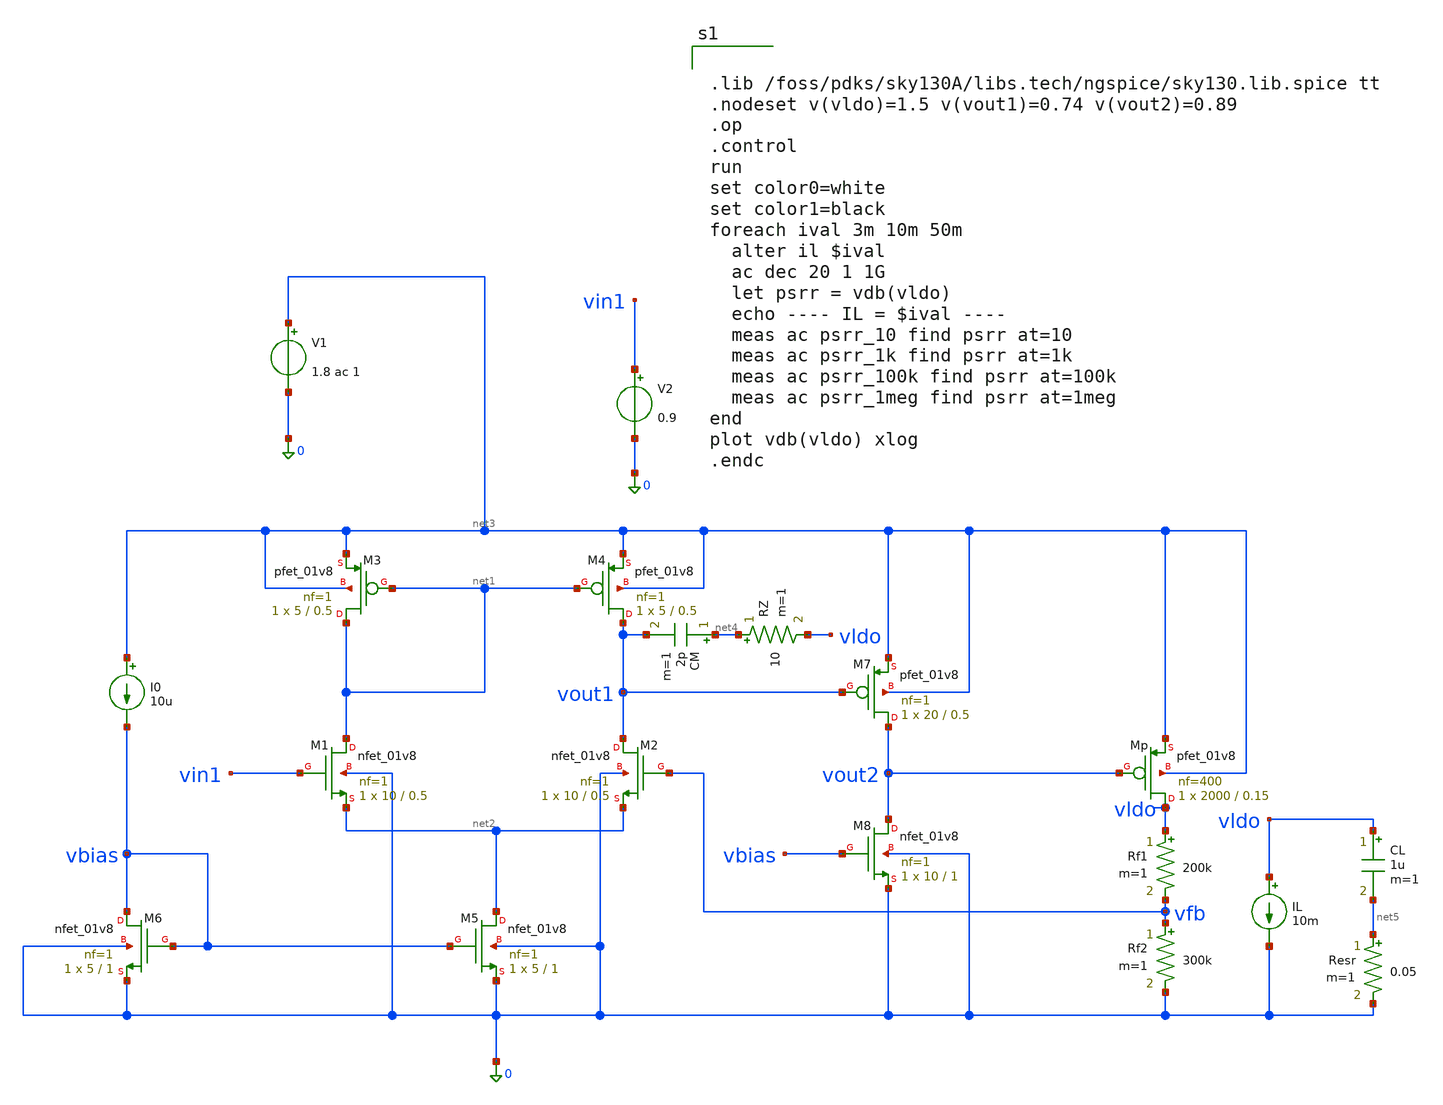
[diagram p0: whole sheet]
** sch_path: src/schematics/ldo_top.sch
**.subckt ldo_top
XM1 net1 vin1 net2 0 sky130_fd_pr__nfet_01v8 L=0.5 W=10 nf=1 ad='int((1 + 1)/2) * 10 / 1 * 0.29' as='int((1 + 2)/2) * 10 / 1 * 0.29'
+ pd='2*int((1 + 1)/2) * (10 / 1 + 0.29)' ps='2*int((1 + 2)/2) * (10 / 1 + 0.29)' nrd='0.29 / 10 ' nrs='0.29 / 10 '
+ sa=0 sb=0 sd=0 mult=1 m=1
XM2 vout1 vfb net2 0 sky130_fd_pr__nfet_01v8 L=0.5 W=10 nf=1 ad='int((1 + 1)/2) * 10 / 1 * 0.29' as='int((1 + 2)/2) * 10 / 1 * 0.29'
+ pd='2*int((1 + 1)/2) * (10 / 1 + 0.29)' ps='2*int((1 + 2)/2) * (10 / 1 + 0.29)' nrd='0.29 / 10 ' nrs='0.29 / 10 '
+ sa=0 sb=0 sd=0 mult=1 m=1
XM3 net1 net1 net3 net3 sky130_fd_pr__pfet_01v8 L=0.5 W=5 nf=1 ad='int((1 + 1)/2) * 5 / 1 * 0.29' as='int((1 + 2)/2) * 5 / 1 * 0.29'
+ pd='2*int((1 + 1)/2) * (5 / 1 + 0.29)' ps='2*int((1 + 2)/2) * (5 / 1 + 0.29)' nrd='0.29 / 5 ' nrs='0.29 / 5 '
+ sa=0 sb=0 sd=0 mult=1 m=1
XM4 vout1 net1 net3 net3 sky130_fd_pr__pfet_01v8 L=0.5 W=5 nf=1 ad='int((1 + 1)/2) * 5 / 1 * 0.29' as='int((1 + 2)/2) * 5 / 1 * 0.29'
+ pd='2*int((1 + 1)/2) * (5 / 1 + 0.29)' ps='2*int((1 + 2)/2) * (5 / 1 + 0.29)' nrd='0.29 / 5 ' nrs='0.29 / 5 '
+ sa=0 sb=0 sd=0 mult=1 m=1
XM5 net2 vbias 0 0 sky130_fd_pr__nfet_01v8 L=1 W=5 nf=1 ad='int((1 + 1)/2) * 5 / 1 * 0.29' as='int((1 + 2)/2) * 5 / 1 * 0.29'
+ pd='2*int((1 + 1)/2) * (5 / 1 + 0.29)' ps='2*int((1 + 2)/2) * (5 / 1 + 0.29)' nrd='0.29 / 5 ' nrs='0.29 / 5 '
+ sa=0 sb=0 sd=0 mult=1 m=1
XM6 vbias vbias 0 0 sky130_fd_pr__nfet_01v8 L=1 W=5 nf=1 ad='int((1 + 1)/2) * 5 / 1 * 0.29' as='int((1 + 2)/2) * 5 / 1 * 0.29'
+ pd='2*int((1 + 1)/2) * (5 / 1 + 0.29)' ps='2*int((1 + 2)/2) * (5 / 1 + 0.29)' nrd='0.29 / 5 ' nrs='0.29 / 5 '
+ sa=0 sb=0 sd=0 mult=1 m=1
I0 net3 vbias 10u
V1 net3 0 1.8 ac 1
V2 vin1 0 0.9
XM7 vout2 vout1 net3 net3 sky130_fd_pr__pfet_01v8 L=0.5 W=20 nf=1 ad='int((1 + 1)/2) * 20 / 1 * 0.29'
+ as='int((1 + 2)/2) * 20 / 1 * 0.29' pd='2*int((1 + 1)/2) * (20 / 1 + 0.29)' ps='2*int((1 + 2)/2) * (20 / 1 + 0.29)'
+ nrd='0.29 / 20 ' nrs='0.29 / 20 ' sa=0 sb=0 sd=0 mult=1 m=1
XM8 vout2 vbias 0 0 sky130_fd_pr__nfet_01v8 L=1 W=10 nf=1 ad='int((1 + 1)/2) * 10 / 1 * 0.29' as='int((1 + 2)/2) * 10 / 1 * 0.29'
+ pd='2*int((1 + 1)/2) * (10 / 1 + 0.29)' ps='2*int((1 + 2)/2) * (10 / 1 + 0.29)' nrd='0.29 / 10 ' nrs='0.29 / 10 '
+ sa=0 sb=0 sd=0 mult=1 m=1
CM net4 vout1 2p m=1
RZ net4 vldo 10 m=1
Rf1 vldo vfb 200k m=1
Rf2 vfb 0 300k m=1
CL vldo net5 1u m=1
IL vldo 0 10m
XMp vldo vout2 net3 net3 sky130_fd_pr__pfet_01v8 L=0.15 W=2000 nf=400 ad='int((400 + 1)/2) * 2000 / 400 * 0.29'
+ as='int((400 + 2)/2) * 2000 / 400 * 0.29' pd='2*int((400 + 1)/2) * (2000 / 400 + 0.29)' ps='2*int((400 + 2)/2) * (2000 / 400 + 0.29)'
+ nrd='0.29 / 2000 ' nrs='0.29 / 2000 ' sa=0 sb=0 sd=0 mult=1 m=1
Resr net5 0 0.05 m=1
**** begin user architecture code


.lib /foss/pdks/sky130A/libs.tech/ngspice/sky130.lib.spice tt
.nodeset v(vldo)=1.5 v(vout1)=0.74 v(vout2)=0.89
.op
.control
run
set color0=white
set color1=black
foreach ival 3m 10m 50m
  alter il $ival
  ac dec 20 1 1G
  let psrr = vdb(vldo)
  echo ---- IL = $ival ----
  meas ac psrr_10 find psrr at=10
  meas ac psrr_1k find psrr at=1k
  meas ac psrr_100k find psrr at=100k
  meas ac psrr_1meg find psrr at=1meg
end
plot vdb(vldo) xlog
.endc


**** end user architecture code
**.ends
.end
